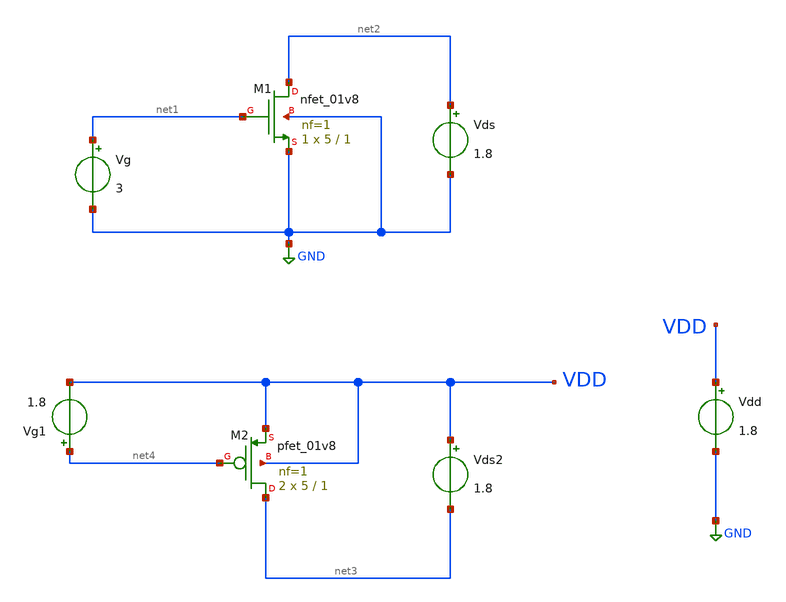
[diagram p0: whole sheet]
** sch_path: xschem/characterization/sim.sch

.lib $::SKYWATER_MODELS/sky130.lib.spice tt
.include $::SKYWATER_STDCELLS/sky130_fd_sc_hd.spice

**.subckt sim
Vg net1 GND 3
Vds net2 GND 1.8
Vg1 net4 VDD 1.8
Vds2 VDD net3 1.8
Vdd VDD GND 1.8
XM2 net3 net4 VDD VDD sky130_fd_pr__pfet_01v8 L=1 W=5 nf=1 ad='W * 0.29' as='W * 0.29' pd='2 * (W + 0.29)'
+ ps='2 * (W + 0.29)' nrd='0.29 / W' nrs='0.29 / W' sa=0 sb=0 sd=0 mult=2 m=2
XM1 net2 net1 GND GND sky130_fd_pr__nfet_01v8 L=1 W=5 nf=1 ad='int((nf+1)/2) * W/nf * 0.29' as='int((nf+2)/2) * W/nf * 0.29'
+ pd='2*int((nf+1)/2) * (W/nf + 0.29)' ps='2*int((nf+2)/2) * (W/nf + 0.29)' nrd='0.29 / W' nrs='0.29 / W'
+ sa=0 sb=0 sd=0 mult=1 m=1
**.ends
.GLOBAL GND
**** begin user architecture code


.options savecurrents
.control
 save all
 op
 write test_analog.raw
.endc


**** end user architecture code
.end
